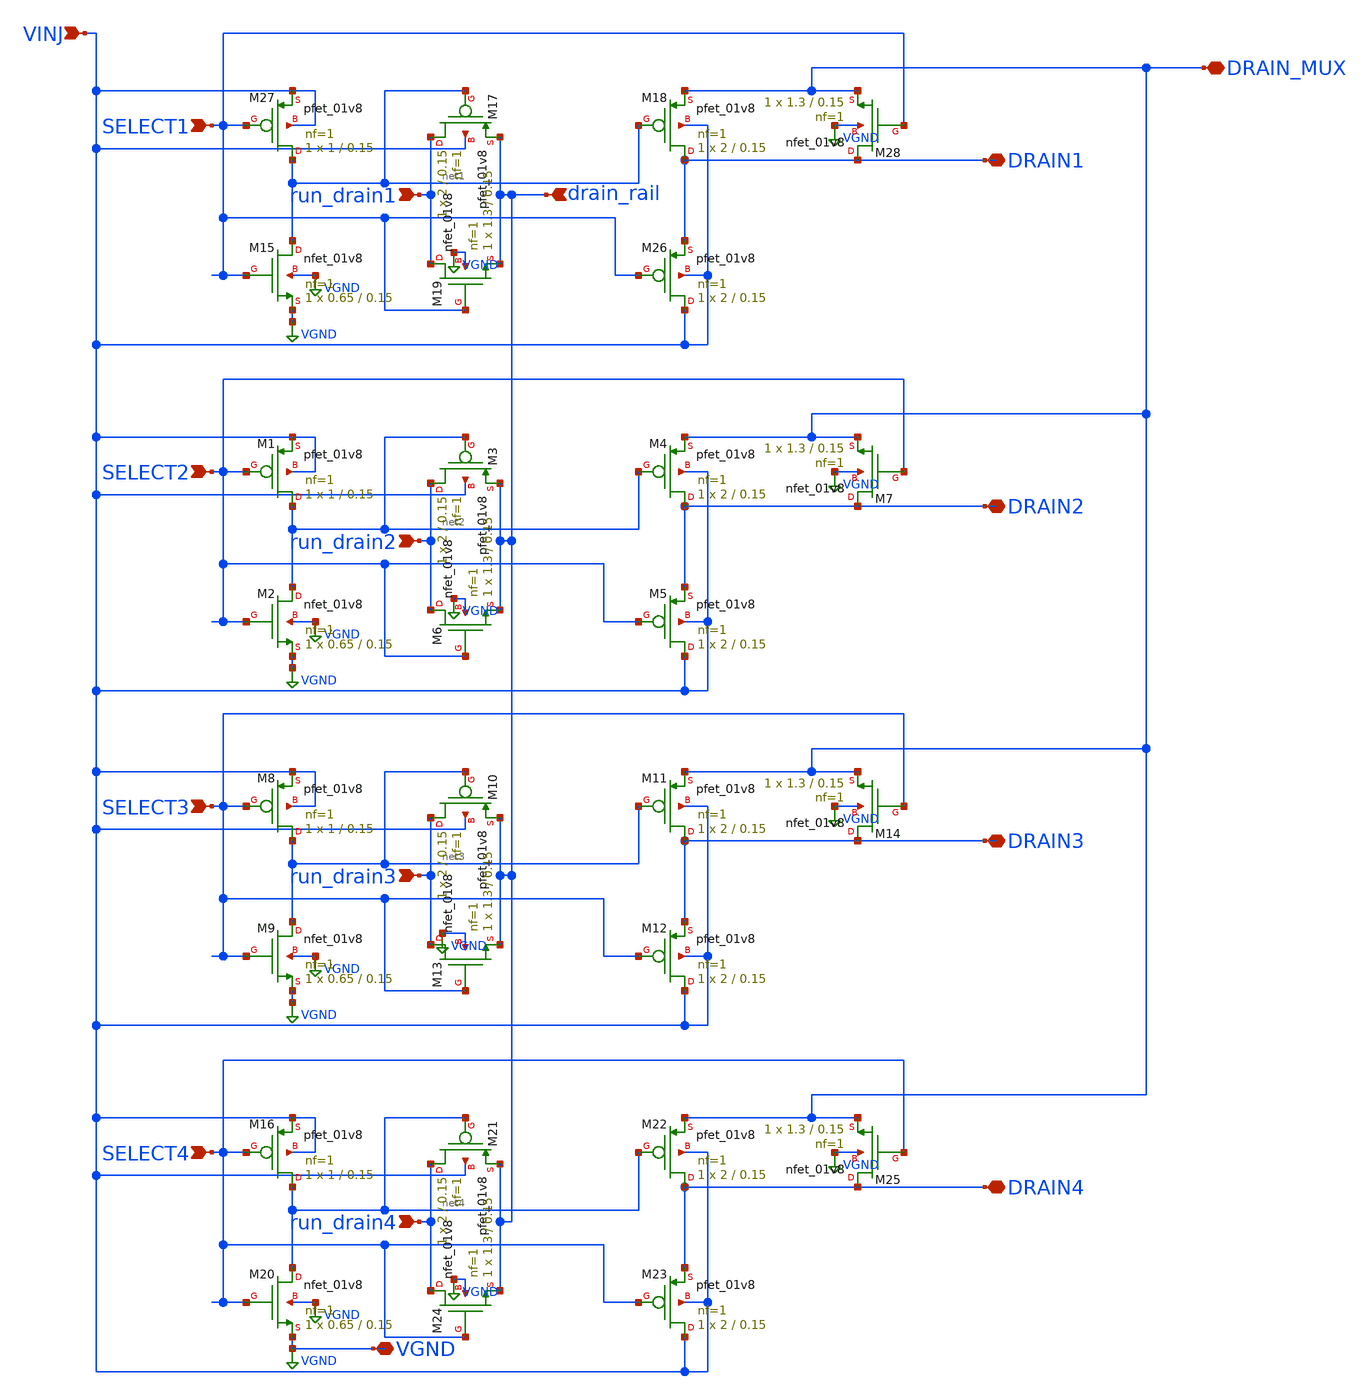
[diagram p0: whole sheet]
** sch_path: sky130_cells/Practice/DrainSelect/DrainSelectSchematic.sch
**.subckt DrainSelectSchematic SELECT1 DRAIN_MUX DRAIN1 VINJ SELECT2 DRAIN2 SELECT3 DRAIN3 SELECT4
*+ DRAIN4 VGND run_drain1 drain_rail run_drain2 run_drain3 run_drain4
*.ipin SELECT1
*.iopin DRAIN_MUX
*.iopin DRAIN1
*.ipin VINJ
*.ipin SELECT2
*.iopin DRAIN2
*.ipin SELECT3
*.iopin DRAIN3
*.ipin SELECT4
*.iopin DRAIN4
*.iopin VGND
*.ipin run_drain1
*.ipin drain_rail
*.ipin run_drain2
*.ipin run_drain3
*.ipin run_drain4
XM27 net1 SELECT1 VINJ VINJ sky130_fd_pr__pfet_01v8 L=0.15 W=1 nf=1 ad='int((1 + 1)/2) * 1 / 1 * 0.29'
+ as='int((1 + 2)/2) * 1 / 1 * 0.29' pd='2*int((1 + 1)/2) * (1 / 1 + 0.29)' ps='2*int((1 + 2)/2) * (1 / 1 + 0.29)'
+ nrd='0.29 / 1 ' nrs='0.29 / 1 ' sa=0 sb=0 sd=0 mult=1 m=1
XM15 net1 SELECT1 VGND VGND sky130_fd_pr__nfet_01v8 L=0.15 W=0.65 nf=1 ad='int((1 + 1)/2) * 0.65 / 1 * 0.29'
+ as='int((1 + 2)/2) * 0.65 / 1 * 0.29' pd='2*int((1 + 1)/2) * (0.65 / 1 + 0.29)' ps='2*int((1 + 2)/2) * (0.65 / 1 + 0.29)'
+ nrd='0.29 / 0.65 ' nrs='0.29 / 0.65 ' sa=0 sb=0 sd=0 mult=1 m=1
XM17 run_drain1 net1 drain_rail VINJ sky130_fd_pr__pfet_01v8 L=0.15 W=2 nf=1 ad='int((1 + 1)/2) * 2 / 1 * 0.29'
+ as='int((1 + 2)/2) * 2 / 1 * 0.29' pd='2*int((1 + 1)/2) * (2 / 1 + 0.29)' ps='2*int((1 + 2)/2) * (2 / 1 + 0.29)'
+ nrd='0.29 / 2 ' nrs='0.29 / 2 ' sa=0 sb=0 sd=0 mult=1 m=1
XM18 DRAIN1 net1 DRAIN_MUX VINJ sky130_fd_pr__pfet_01v8 L=0.15 W=2 nf=1 ad='int((1 + 1)/2) * 2 / 1 * 0.29'
+ as='int((1 + 2)/2) * 2 / 1 * 0.29' pd='2*int((1 + 1)/2) * (2 / 1 + 0.29)' ps='2*int((1 + 2)/2) * (2 / 1 + 0.29)'
+ nrd='0.29 / 2 ' nrs='0.29 / 2 ' sa=0 sb=0 sd=0 mult=1 m=1
XM26 VINJ SELECT1 DRAIN1 VINJ sky130_fd_pr__pfet_01v8 L=0.15 W=2 nf=1 ad='int((1 + 1)/2) * 2 / 1 * 0.29'
+ as='int((1 + 2)/2) * 2 / 1 * 0.29' pd='2*int((1 + 1)/2) * (2 / 1 + 0.29)' ps='2*int((1 + 2)/2) * (2 / 1 + 0.29)'
+ nrd='0.29 / 2 ' nrs='0.29 / 2 ' sa=0 sb=0 sd=0 mult=1 m=1
XM19 run_drain1 SELECT1 drain_rail VGND sky130_fd_pr__nfet_01v8 L=0.15 W=1.3 nf=1 ad='int((1 + 1)/2) * 1.3 / 1 * 0.29'
+ as='int((1 + 2)/2) * 1.3 / 1 * 0.29' pd='2*int((1 + 1)/2) * (1.3 / 1 + 0.29)' ps='2*int((1 + 2)/2) * (1.3 / 1 + 0.29)'
+ nrd='0.29 / 1.3 ' nrs='0.29 / 1.3 ' sa=0 sb=0 sd=0 mult=1 m=1
XM28 DRAIN1 SELECT1 DRAIN_MUX VGND sky130_fd_pr__nfet_01v8 L=0.15 W=1.3 nf=1 ad='int((1 + 1)/2) * 1.3 / 1 * 0.29'
+ as='int((1 + 2)/2) * 1.3 / 1 * 0.29' pd='2*int((1 + 1)/2) * (1.3 / 1 + 0.29)' ps='2*int((1 + 2)/2) * (1.3 / 1 + 0.29)'
+ nrd='0.29 / 1.3 ' nrs='0.29 / 1.3 ' sa=0 sb=0 sd=0 mult=1 m=1
XM1 net2 SELECT2 VINJ VINJ sky130_fd_pr__pfet_01v8 L=0.15 W=1 nf=1 ad='int((1 + 1)/2) * 1 / 1 * 0.29'
+ as='int((1 + 2)/2) * 1 / 1 * 0.29' pd='2*int((1 + 1)/2) * (1 / 1 + 0.29)' ps='2*int((1 + 2)/2) * (1 / 1 + 0.29)'
+ nrd='0.29 / 1 ' nrs='0.29 / 1 ' sa=0 sb=0 sd=0 mult=1 m=1
XM2 net2 SELECT2 VGND VGND sky130_fd_pr__nfet_01v8 L=0.15 W=0.65 nf=1 ad='int((1 + 1)/2) * 0.65 / 1 * 0.29'
+ as='int((1 + 2)/2) * 0.65 / 1 * 0.29' pd='2*int((1 + 1)/2) * (0.65 / 1 + 0.29)' ps='2*int((1 + 2)/2) * (0.65 / 1 + 0.29)'
+ nrd='0.29 / 0.65 ' nrs='0.29 / 0.65 ' sa=0 sb=0 sd=0 mult=1 m=1
XM3 run_drain2 net2 drain_rail VINJ sky130_fd_pr__pfet_01v8 L=0.15 W=2 nf=1 ad='int((1 + 1)/2) * 2 / 1 * 0.29'
+ as='int((1 + 2)/2) * 2 / 1 * 0.29' pd='2*int((1 + 1)/2) * (2 / 1 + 0.29)' ps='2*int((1 + 2)/2) * (2 / 1 + 0.29)'
+ nrd='0.29 / 2 ' nrs='0.29 / 2 ' sa=0 sb=0 sd=0 mult=1 m=1
XM4 DRAIN2 net2 DRAIN_MUX VINJ sky130_fd_pr__pfet_01v8 L=0.15 W=2 nf=1 ad='int((1 + 1)/2) * 2 / 1 * 0.29'
+ as='int((1 + 2)/2) * 2 / 1 * 0.29' pd='2*int((1 + 1)/2) * (2 / 1 + 0.29)' ps='2*int((1 + 2)/2) * (2 / 1 + 0.29)'
+ nrd='0.29 / 2 ' nrs='0.29 / 2 ' sa=0 sb=0 sd=0 mult=1 m=1
XM5 VINJ SELECT2 DRAIN2 VINJ sky130_fd_pr__pfet_01v8 L=0.15 W=2 nf=1 ad='int((1 + 1)/2) * 2 / 1 * 0.29'
+ as='int((1 + 2)/2) * 2 / 1 * 0.29' pd='2*int((1 + 1)/2) * (2 / 1 + 0.29)' ps='2*int((1 + 2)/2) * (2 / 1 + 0.29)'
+ nrd='0.29 / 2 ' nrs='0.29 / 2 ' sa=0 sb=0 sd=0 mult=1 m=1
XM6 run_drain2 SELECT2 drain_rail VGND sky130_fd_pr__nfet_01v8 L=0.15 W=1.3 nf=1 ad='int((1 + 1)/2) * 1.3 / 1 * 0.29'
+ as='int((1 + 2)/2) * 1.3 / 1 * 0.29' pd='2*int((1 + 1)/2) * (1.3 / 1 + 0.29)' ps='2*int((1 + 2)/2) * (1.3 / 1 + 0.29)'
+ nrd='0.29 / 1.3 ' nrs='0.29 / 1.3 ' sa=0 sb=0 sd=0 mult=1 m=1
XM7 DRAIN2 SELECT2 DRAIN_MUX VGND sky130_fd_pr__nfet_01v8 L=0.15 W=1.3 nf=1 ad='int((1 + 1)/2) * 1.3 / 1 * 0.29'
+ as='int((1 + 2)/2) * 1.3 / 1 * 0.29' pd='2*int((1 + 1)/2) * (1.3 / 1 + 0.29)' ps='2*int((1 + 2)/2) * (1.3 / 1 + 0.29)'
+ nrd='0.29 / 1.3 ' nrs='0.29 / 1.3 ' sa=0 sb=0 sd=0 mult=1 m=1
XM8 net3 SELECT3 VINJ VINJ sky130_fd_pr__pfet_01v8 L=0.15 W=1 nf=1 ad='int((1 + 1)/2) * 1 / 1 * 0.29'
+ as='int((1 + 2)/2) * 1 / 1 * 0.29' pd='2*int((1 + 1)/2) * (1 / 1 + 0.29)' ps='2*int((1 + 2)/2) * (1 / 1 + 0.29)'
+ nrd='0.29 / 1 ' nrs='0.29 / 1 ' sa=0 sb=0 sd=0 mult=1 m=1
XM9 net3 SELECT3 VGND VGND sky130_fd_pr__nfet_01v8 L=0.15 W=0.65 nf=1 ad='int((1 + 1)/2) * 0.65 / 1 * 0.29'
+ as='int((1 + 2)/2) * 0.65 / 1 * 0.29' pd='2*int((1 + 1)/2) * (0.65 / 1 + 0.29)' ps='2*int((1 + 2)/2) * (0.65 / 1 + 0.29)'
+ nrd='0.29 / 0.65 ' nrs='0.29 / 0.65 ' sa=0 sb=0 sd=0 mult=1 m=1
XM10 run_drain3 net3 drain_rail VINJ sky130_fd_pr__pfet_01v8 L=0.15 W=2 nf=1 ad='int((1 + 1)/2) * 2 / 1 * 0.29'
+ as='int((1 + 2)/2) * 2 / 1 * 0.29' pd='2*int((1 + 1)/2) * (2 / 1 + 0.29)' ps='2*int((1 + 2)/2) * (2 / 1 + 0.29)'
+ nrd='0.29 / 2 ' nrs='0.29 / 2 ' sa=0 sb=0 sd=0 mult=1 m=1
XM11 DRAIN3 net3 DRAIN_MUX VINJ sky130_fd_pr__pfet_01v8 L=0.15 W=2 nf=1 ad='int((1 + 1)/2) * 2 / 1 * 0.29'
+ as='int((1 + 2)/2) * 2 / 1 * 0.29' pd='2*int((1 + 1)/2) * (2 / 1 + 0.29)' ps='2*int((1 + 2)/2) * (2 / 1 + 0.29)'
+ nrd='0.29 / 2 ' nrs='0.29 / 2 ' sa=0 sb=0 sd=0 mult=1 m=1
XM12 VINJ SELECT3 DRAIN3 VINJ sky130_fd_pr__pfet_01v8 L=0.15 W=2 nf=1 ad='int((1 + 1)/2) * 2 / 1 * 0.29'
+ as='int((1 + 2)/2) * 2 / 1 * 0.29' pd='2*int((1 + 1)/2) * (2 / 1 + 0.29)' ps='2*int((1 + 2)/2) * (2 / 1 + 0.29)'
+ nrd='0.29 / 2 ' nrs='0.29 / 2 ' sa=0 sb=0 sd=0 mult=1 m=1
XM13 run_drain3 SELECT3 drain_rail VGND sky130_fd_pr__nfet_01v8 L=0.15 W=1.3 nf=1 ad='int((1 + 1)/2) * 1.3 / 1 * 0.29'
+ as='int((1 + 2)/2) * 1.3 / 1 * 0.29' pd='2*int((1 + 1)/2) * (1.3 / 1 + 0.29)' ps='2*int((1 + 2)/2) * (1.3 / 1 + 0.29)'
+ nrd='0.29 / 1.3 ' nrs='0.29 / 1.3 ' sa=0 sb=0 sd=0 mult=1 m=1
XM14 DRAIN3 SELECT3 DRAIN_MUX VGND sky130_fd_pr__nfet_01v8 L=0.15 W=1.3 nf=1 ad='int((1 + 1)/2) * 1.3 / 1 * 0.29'
+ as='int((1 + 2)/2) * 1.3 / 1 * 0.29' pd='2*int((1 + 1)/2) * (1.3 / 1 + 0.29)' ps='2*int((1 + 2)/2) * (1.3 / 1 + 0.29)'
+ nrd='0.29 / 1.3 ' nrs='0.29 / 1.3 ' sa=0 sb=0 sd=0 mult=1 m=1
XM16 net4 SELECT4 VINJ VINJ sky130_fd_pr__pfet_01v8 L=0.15 W=1 nf=1 ad='int((1 + 1)/2) * 1 / 1 * 0.29'
+ as='int((1 + 2)/2) * 1 / 1 * 0.29' pd='2*int((1 + 1)/2) * (1 / 1 + 0.29)' ps='2*int((1 + 2)/2) * (1 / 1 + 0.29)'
+ nrd='0.29 / 1 ' nrs='0.29 / 1 ' sa=0 sb=0 sd=0 mult=1 m=1
XM20 net4 SELECT4 VGND VGND sky130_fd_pr__nfet_01v8 L=0.15 W=0.65 nf=1 ad='int((1 + 1)/2) * 0.65 / 1 * 0.29'
+ as='int((1 + 2)/2) * 0.65 / 1 * 0.29' pd='2*int((1 + 1)/2) * (0.65 / 1 + 0.29)' ps='2*int((1 + 2)/2) * (0.65 / 1 + 0.29)'
+ nrd='0.29 / 0.65 ' nrs='0.29 / 0.65 ' sa=0 sb=0 sd=0 mult=1 m=1
XM21 run_drain4 net4 drain_rail VINJ sky130_fd_pr__pfet_01v8 L=0.15 W=2 nf=1 ad='int((1 + 1)/2) * 2 / 1 * 0.29'
+ as='int((1 + 2)/2) * 2 / 1 * 0.29' pd='2*int((1 + 1)/2) * (2 / 1 + 0.29)' ps='2*int((1 + 2)/2) * (2 / 1 + 0.29)'
+ nrd='0.29 / 2 ' nrs='0.29 / 2 ' sa=0 sb=0 sd=0 mult=1 m=1
XM22 DRAIN4 net4 DRAIN_MUX VINJ sky130_fd_pr__pfet_01v8 L=0.15 W=2 nf=1 ad='int((1 + 1)/2) * 2 / 1 * 0.29'
+ as='int((1 + 2)/2) * 2 / 1 * 0.29' pd='2*int((1 + 1)/2) * (2 / 1 + 0.29)' ps='2*int((1 + 2)/2) * (2 / 1 + 0.29)'
+ nrd='0.29 / 2 ' nrs='0.29 / 2 ' sa=0 sb=0 sd=0 mult=1 m=1
XM23 VINJ SELECT4 DRAIN4 VINJ sky130_fd_pr__pfet_01v8 L=0.15 W=2 nf=1 ad='int((1 + 1)/2) * 2 / 1 * 0.29'
+ as='int((1 + 2)/2) * 2 / 1 * 0.29' pd='2*int((1 + 1)/2) * (2 / 1 + 0.29)' ps='2*int((1 + 2)/2) * (2 / 1 + 0.29)'
+ nrd='0.29 / 2 ' nrs='0.29 / 2 ' sa=0 sb=0 sd=0 mult=1 m=1
XM24 run_drain4 SELECT4 drain_rail VGND sky130_fd_pr__nfet_01v8 L=0.15 W=1.3 nf=1 ad='int((1 + 1)/2) * 1.3 / 1 * 0.29'
+ as='int((1 + 2)/2) * 1.3 / 1 * 0.29' pd='2*int((1 + 1)/2) * (1.3 / 1 + 0.29)' ps='2*int((1 + 2)/2) * (1.3 / 1 + 0.29)'
+ nrd='0.29 / 1.3 ' nrs='0.29 / 1.3 ' sa=0 sb=0 sd=0 mult=1 m=1
XM25 DRAIN4 SELECT4 DRAIN_MUX VGND sky130_fd_pr__nfet_01v8 L=0.15 W=1.3 nf=1 ad='int((1 + 1)/2) * 1.3 / 1 * 0.29'
+ as='int((1 + 2)/2) * 1.3 / 1 * 0.29' pd='2*int((1 + 1)/2) * (1.3 / 1 + 0.29)' ps='2*int((1 + 2)/2) * (1.3 / 1 + 0.29)'
+ nrd='0.29 / 1.3 ' nrs='0.29 / 1.3 ' sa=0 sb=0 sd=0 mult=1 m=1
**.ends
.GLOBAL VGND
.end
